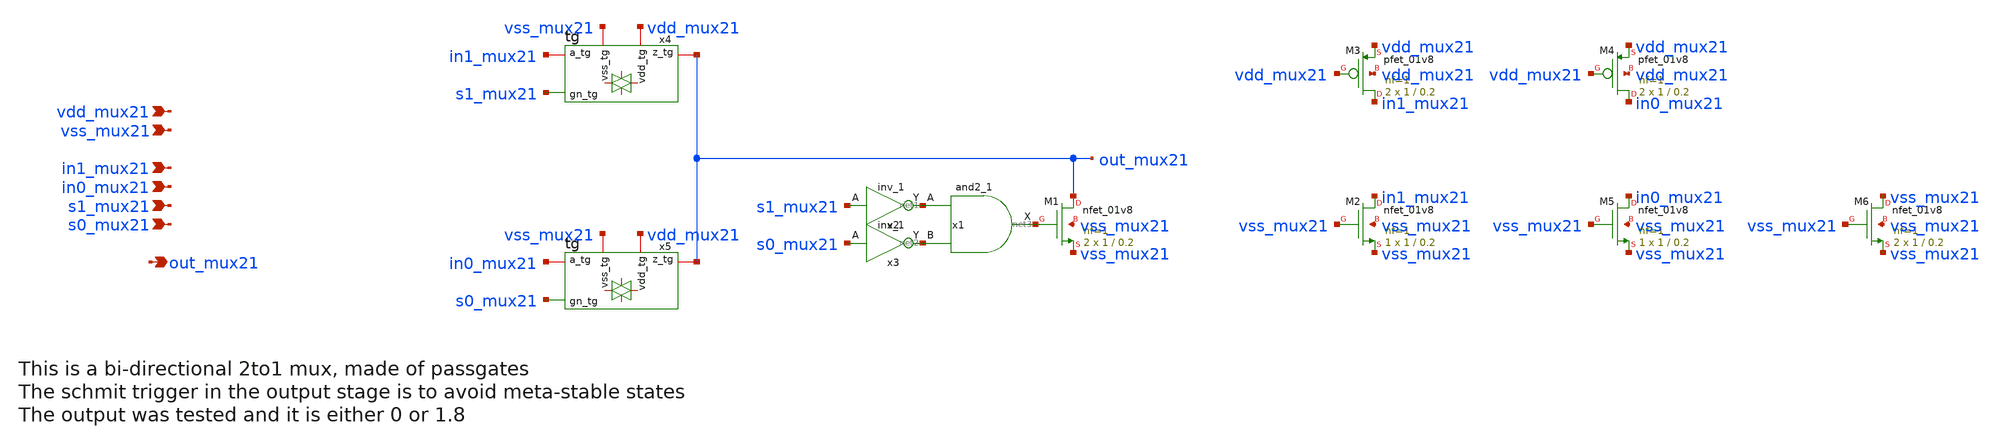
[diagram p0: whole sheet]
** sch_path: mux21.sch
**.subckt mux21 vdd_mux21 vss_mux21 in1_mux21 in0_mux21 out_mux21 s1_mux21 s0_mux21
*.ipin vdd_mux21
*.ipin vss_mux21
*.ipin in1_mux21
*.ipin in0_mux21
*.opin out_mux21
*.ipin s1_mux21
*.ipin s0_mux21
x1 net1 net2 vss_mux21 vss_mux21 vdd_mux21 vdd_mux21 net3 sky130_fd_sc_hd__and2_1
XM1 out_mux21 net3 vss_mux21 vss_mux21 sky130_fd_pr__nfet_01v8 L=0.2 W=1 nf=1 ad='int((nf+1)/2) * W/nf * 0.29'
+ as='int((nf+2)/2) * W/nf * 0.29' pd='2*int((nf+1)/2) * (W/nf + 0.29)' ps='2*int((nf+2)/2) * (W/nf + 0.29)'
+ nrd='0.29 / W' nrs='0.29 / W' sa=0 sb=0 sd=0 mult=2 m=2
x2 s1_mux21 vss_mux21 vss_mux21 vdd_mux21 vdd_mux21 net1 sky130_fd_sc_hd__inv_1
x3 s0_mux21 vss_mux21 vss_mux21 vdd_mux21 vdd_mux21 net2 sky130_fd_sc_hd__inv_1
x4 vdd_mux21 in1_mux21 out_mux21 vss_mux21 s1_mux21 tg
x5 vdd_mux21 in0_mux21 out_mux21 vss_mux21 s0_mux21 tg
XM2 in1_mux21 vss_mux21 vss_mux21 vss_mux21 sky130_fd_pr__nfet_01v8 L=0.2 W=1 nf=1 ad='int((nf+1)/2) * W/nf * 0.29'
+ as='int((nf+2)/2) * W/nf * 0.29' pd='2*int((nf+1)/2) * (W/nf + 0.29)' ps='2*int((nf+2)/2) * (W/nf + 0.29)'
+ nrd='0.29 / W' nrs='0.29 / W' sa=0 sb=0 sd=0 mult=1 m=1
XM3 in1_mux21 vdd_mux21 vdd_mux21 vdd_mux21 sky130_fd_pr__pfet_01v8 L=0.2 W=1 nf=1 ad='int((nf+1)/2) * W/nf * 0.29'
+ as='int((nf+2)/2) * W/nf * 0.29' pd='2*int((nf+1)/2) * (W/nf + 0.29)' ps='2*int((nf+2)/2) * (W/nf + 0.29)'
+ nrd='0.29 / W' nrs='0.29 / W' sa=0 sb=0 sd=0 mult=2 m=2
XM4 in0_mux21 vdd_mux21 vdd_mux21 vdd_mux21 sky130_fd_pr__pfet_01v8 L=0.2 W=1 nf=1 ad='int((nf+1)/2) * W/nf * 0.29'
+ as='int((nf+2)/2) * W/nf * 0.29' pd='2*int((nf+1)/2) * (W/nf + 0.29)' ps='2*int((nf+2)/2) * (W/nf + 0.29)'
+ nrd='0.29 / W' nrs='0.29 / W' sa=0 sb=0 sd=0 mult=2 m=2
XM5 in0_mux21 vss_mux21 vss_mux21 vss_mux21 sky130_fd_pr__nfet_01v8 L=0.2 W=1 nf=1 ad='int((nf+1)/2) * W/nf * 0.29'
+ as='int((nf+2)/2) * W/nf * 0.29' pd='2*int((nf+1)/2) * (W/nf + 0.29)' ps='2*int((nf+2)/2) * (W/nf + 0.29)'
+ nrd='0.29 / W' nrs='0.29 / W' sa=0 sb=0 sd=0 mult=1 m=1
XM6 vss_mux21 vss_mux21 vss_mux21 vss_mux21 sky130_fd_pr__nfet_01v8 L=0.2 W=1 nf=1 ad='int((nf+1)/2) * W/nf * 0.29'
+ as='int((nf+2)/2) * W/nf * 0.29' pd='2*int((nf+1)/2) * (W/nf + 0.29)' ps='2*int((nf+2)/2) * (W/nf + 0.29)'
+ nrd='0.29 / W' nrs='0.29 / W' sa=0 sb=0 sd=0 mult=2 m=2
**.ends

* expanding   symbol:  tg.sym # of pins=5
** sym_path: tg.sym
** sch_path: tg.sch
.subckt tg vdd_tg a_tg z_tg vss_tg gn_tg
*.iopin a_tg
*.iopin z_tg
*.ipin gn_tg
*.iopin vss_tg
*.iopin vdd_tg
XM1 a_tg gn_tg z_tg vss_tg sky130_fd_pr__nfet_01v8 L=0.2 W=1 nf=1 ad='int((nf+1)/2) * W/nf * 0.29' as='int((nf+2)/2) * W/nf * 0.29'
+ pd='2*int((nf+1)/2) * (W/nf + 0.29)' ps='2*int((nf+2)/2) * (W/nf + 0.29)' nrd='0.29 / W' nrs='0.29 / W'
+ sa=0 sb=0 sd=0 mult=1 m=1
XM2 a_tg net1 z_tg vdd_tg sky130_fd_pr__pfet_01v8 L=0.2 W=2 nf=2 ad='int((nf+1)/2) * W/nf * 0.29' as='int((nf+2)/2) * W/nf * 0.29'
+ pd='2*int((nf+1)/2) * (W/nf + 0.29)' ps='2*int((nf+2)/2) * (W/nf + 0.29)' nrd='0.29 / W' nrs='0.29 / W'
+ sa=0 sb=0 sd=0 mult=1 m=1
x10 gn_tg vss_tg vss_tg vdd_tg vdd_tg net1 sky130_fd_sc_hd__inv_1
.ends

.end
